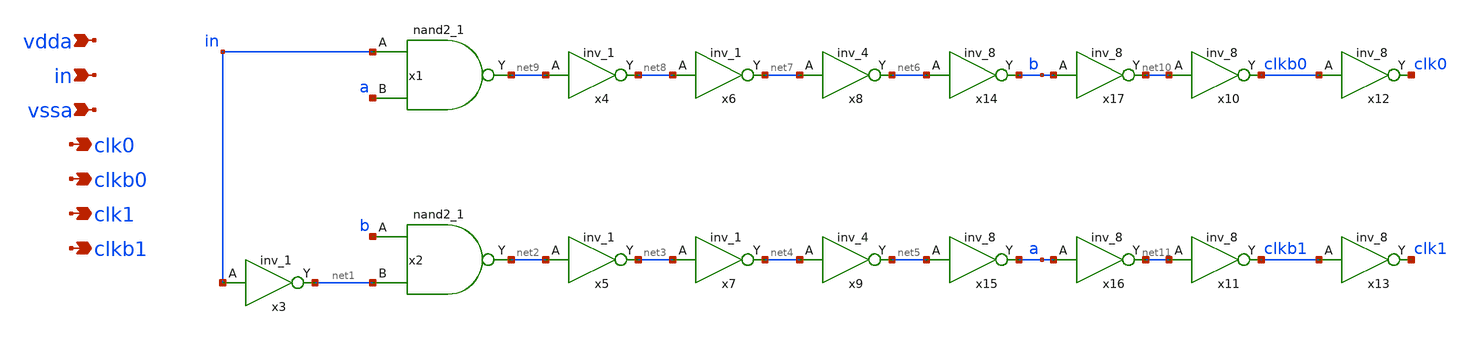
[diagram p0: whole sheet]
** sch_path: xschem/nooverlap_clk.sch
**.subckt nooverlap_clk vdda in vssa clk0 clkb0 clk1 clkb1
*.ipin vdda
*.ipin in
*.ipin vssa
*.opin clk0
*.opin clkb0
*.opin clk1
*.opin clkb1
x1 in a vssa vssa vdda vdda net9 sky130_fd_sc_hd__nand2_1
x2 b net1 vssa vssa vdda vdda net2 sky130_fd_sc_hd__nand2_1
x3 in vssa vssa vdda vdda net1 sky130_fd_sc_hd__inv_1
x4 net9 vssa vssa vdda vdda net8 sky130_fd_sc_hd__inv_1
x5 net2 vssa vssa vdda vdda net3 sky130_fd_sc_hd__inv_1
x6 net8 vssa vssa vdda vdda net7 sky130_fd_sc_hd__inv_1
x7 net3 vssa vssa vdda vdda net4 sky130_fd_sc_hd__inv_1
x8 net7 vssa vssa vdda vdda net6 sky130_fd_sc_hd__inv_4
x9 net4 vssa vssa vdda vdda net5 sky130_fd_sc_hd__inv_4
x10 net10 vssa vssa vdda vdda clkb0 sky130_fd_sc_hd__inv_8
x11 net11 vssa vssa vdda vdda clkb1 sky130_fd_sc_hd__inv_8
x12 clkb0 vssa vssa vdda vdda clk0 sky130_fd_sc_hd__inv_8
x13 clkb1 vssa vssa vdda vdda clk1 sky130_fd_sc_hd__inv_8
x14 net6 vssa vssa vdda vdda b sky130_fd_sc_hd__inv_8
x15 net5 vssa vssa vdda vdda a sky130_fd_sc_hd__inv_8
x16 a vssa vssa vdda vdda net11 sky130_fd_sc_hd__inv_8
x17 b vssa vssa vdda vdda net10 sky130_fd_sc_hd__inv_8
**.ends
.end
